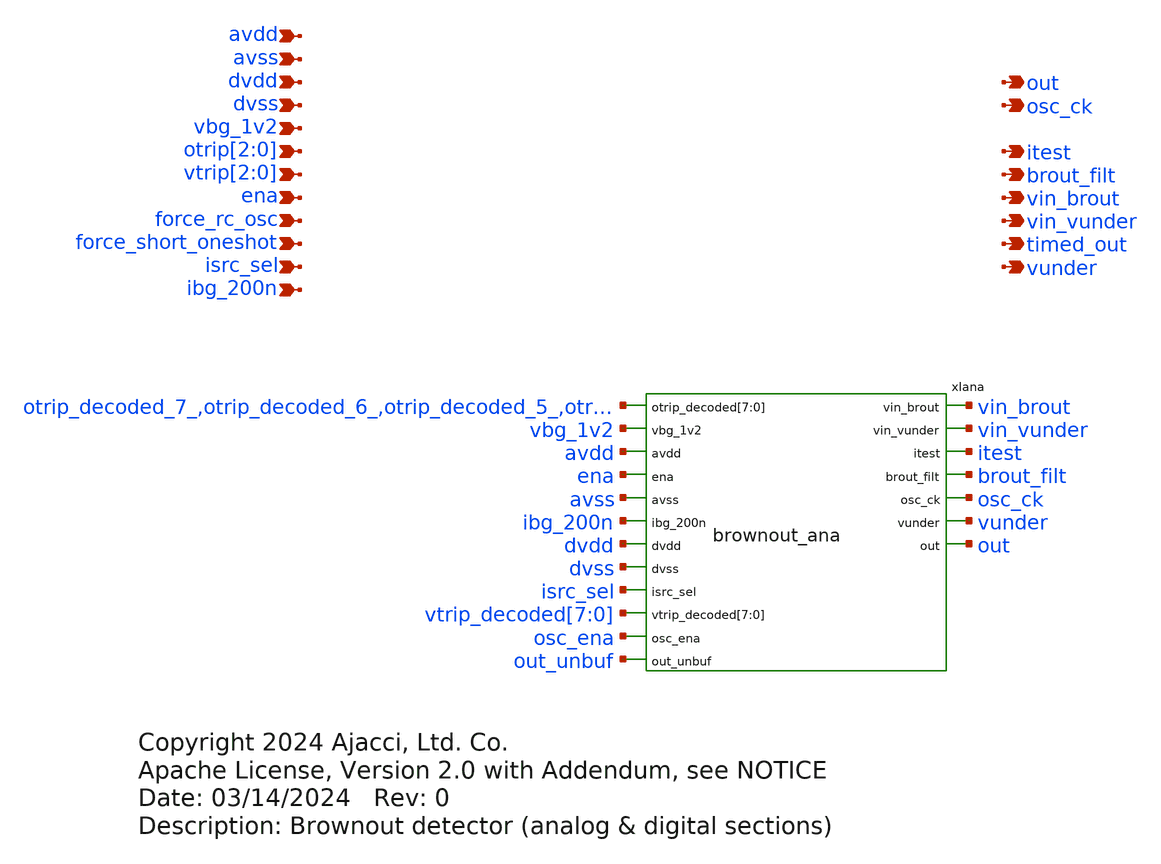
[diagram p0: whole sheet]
** sch_path: xschem/brownout.sch
* Copyright 2024 Ajacci, Ltd. Co.
* Apache License, Version 2.0 with Addendum, see NOTICE
**.subckt brownout avdd avss dvdd dvss vbg_1v2 otrip[2],otrip[1],otrip[0] ena force_rc_osc
*+ force_short_oneshot isrc_sel ibg_200n vin_brout out osc_ck brout_filt itest timed_out vtrip[2],vtrip[1],vtrip[0]
*+ vin_vunder vunder
*.ipin avdd
*.ipin avss
*.ipin dvdd
*.ipin dvss
*.ipin vbg_1v2
*.ipin otrip[2],otrip[1],otrip[0]
*.ipin ena
*.ipin force_rc_osc
*.ipin force_short_oneshot
*.ipin isrc_sel
*.ipin ibg_200n
*.opin vin_brout
*.opin out
*.opin osc_ck
*.opin brout_filt
*.opin itest
*.opin timed_out
*.ipin vtrip[2],vtrip[1],vtrip[0]
*.opin vin_vunder
*.opin vunder
xIana vin_brout vin_vunder otrip_decoded_7_ otrip_decoded_6_ otrip_decoded_5_ otrip_decoded_4_
+ otrip_decoded_3_ otrip_decoded_2_ otrip_decoded_1_ otrip_decoded_0_ vbg_1v2 avdd itest ena avss ibg_200n dvdd dvss
+ isrc_sel vtrip_decoded[7] vtrip_decoded[6] vtrip_decoded[5] vtrip_decoded[4] vtrip_decoded[3]
+ vtrip_decoded[2] vtrip_decoded[1] vtrip_decoded[0] brout_filt osc_ck osc_ena vunder out out_unbuf brownout_ana
**** begin user architecture code



r0 otrip[0] otrip0 1
r1 otrip[1] otrip1 1
r2 otrip[2] otrip2 1
r3 vtrip[0] vtrip0 1
r4 vtrip[1] vtrip1 1
r5 vtrip[2] vtrip2 1

*XSPICE CO-SIM netlist
.include brownout_dig.out.spice
xibrownout_dig dvss dvdd brout_filt ena force_rc_osc force_short_oneshot osc_ck osc_ena  otrip0
+ otrip1 otrip2 otrip_decoded_0_ otrip_decoded_1_ otrip_decoded_2_ otrip_decoded_3_ otrip_decoded_4_
+ otrip_decoded_5_ otrip_decoded_6_ otrip_decoded_7_ out_unbuf timed_out vtrip0 vtrip1 vtrip2 vtrip_decoded_0_
+ vtrip_decoded_1_ vtrip_decoded_2_ vtrip_decoded_3_ vtrip_decoded_4_ vtrip_decoded_5_ vtrip_decoded_6_
+ vtrip_decoded_7_ brownout_dig


**** end user architecture code
**.ends
.end
